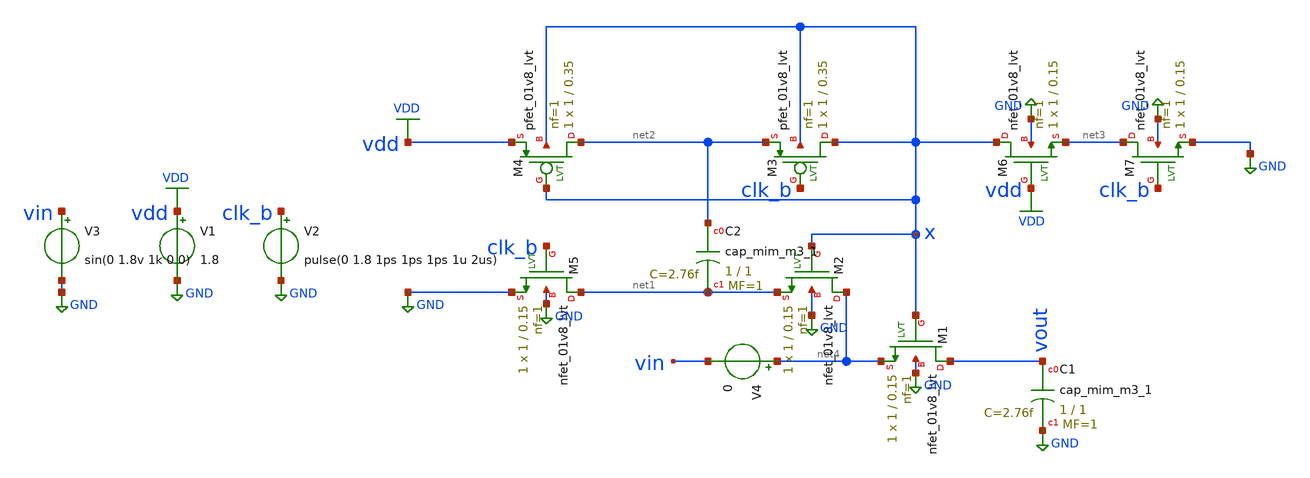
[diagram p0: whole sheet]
** sch_path: bootstrap.sch
**.subckt bootstrap
XM1 vout x net4 GND sky130_fd_pr__nfet_01v8_lvt L=0.15 W=1 nf=1 ad='int((nf+1)/2) * W/nf * 0.29' as='int((nf+2)/2) * W/nf * 0.29'
+ pd='2*int((nf+1)/2) * (W/nf + 0.29)' ps='2*int((nf+2)/2) * (W/nf + 0.29)' nrd='0.29 / W' nrs='0.29 / W'
+ sa=0 sb=0 sd=0 mult=1 m=1
XC1 vout GND sky130_fd_pr__cap_mim_m3_1 W=1 L=1 MF=1 m=1
XM2 net4 x net1 GND sky130_fd_pr__nfet_01v8_lvt L=0.15 W=1 nf=1 ad='int((nf+1)/2) * W/nf * 0.29' as='int((nf+2)/2) * W/nf * 0.29'
+ pd='2*int((nf+1)/2) * (W/nf + 0.29)' ps='2*int((nf+2)/2) * (W/nf + 0.29)' nrd='0.29 / W' nrs='0.29 / W'
+ sa=0 sb=0 sd=0 mult=1 m=1
XC2 net2 net1 sky130_fd_pr__cap_mim_m3_1 W=1 L=1 MF=1 m=1
XM3 x clk_b net2 x sky130_fd_pr__pfet_01v8_lvt L=0.35 W=1 nf=1 ad='int((nf+1)/2) * W/nf * 0.29' as='int((nf+2)/2) * W/nf * 0.29'
+ pd='2*int((nf+1)/2) * (W/nf + 0.29)' ps='2*int((nf+2)/2) * (W/nf + 0.29)' nrd='0.29 / W' nrs='0.29 / W'
+ sa=0 sb=0 sd=0 mult=1 m=1
XM4 net2 x VDD x sky130_fd_pr__pfet_01v8_lvt L=0.35 W=1 nf=1 ad='int((nf+1)/2) * W/nf * 0.29' as='int((nf+2)/2) * W/nf * 0.29'
+ pd='2*int((nf+1)/2) * (W/nf + 0.29)' ps='2*int((nf+2)/2) * (W/nf + 0.29)' nrd='0.29 / W' nrs='0.29 / W'
+ sa=0 sb=0 sd=0 mult=1 m=1
XM5 net1 clk_b GND GND sky130_fd_pr__nfet_01v8_lvt L=0.15 W=1 nf=1 ad='int((nf+1)/2) * W/nf * 0.29' as='int((nf+2)/2) * W/nf * 0.29'
+ pd='2*int((nf+1)/2) * (W/nf + 0.29)' ps='2*int((nf+2)/2) * (W/nf + 0.29)' nrd='0.29 / W' nrs='0.29 / W'
+ sa=0 sb=0 sd=0 mult=1 m=1
XM6 x VDD net3 GND sky130_fd_pr__nfet_01v8_lvt L=0.15 W=1 nf=1 ad='int((nf+1)/2) * W/nf * 0.29' as='int((nf+2)/2) * W/nf * 0.29'
+ pd='2*int((nf+1)/2) * (W/nf + 0.29)' ps='2*int((nf+2)/2) * (W/nf + 0.29)' nrd='0.29 / W' nrs='0.29 / W'
+ sa=0 sb=0 sd=0 mult=1 m=1
XM7 net3 clk_b GND GND sky130_fd_pr__nfet_01v8_lvt L=0.15 W=1 nf=1 ad='int((nf+1)/2) * W/nf * 0.29' as='int((nf+2)/2) * W/nf * 0.29'
+ pd='2*int((nf+1)/2) * (W/nf + 0.29)' ps='2*int((nf+2)/2) * (W/nf + 0.29)' nrd='0.29 / W' nrs='0.29 / W'
+ sa=0 sb=0 sd=0 mult=1 m=1
V1 VDD GND 1.8
V2 clk_b GND pulse(0 1.8 1ps 1ps 1ps 1u 2us)
V3 vin GND sin(0 1.8v 1k 0 0)
V4 net4 vin 0
**** begin user architecture code

.lib ~/open_pdks/sky130/sky130A/libs.tech/ngspice/sky130.lib.spice tt
*.param mc_mm_switch=0
*.param mc_pr_switch=0

*.include ~/open_pdks/sky130/sky130A/libs.tech/ngspice/corners/tt/nonfet.spice

*model
*.include ~/open_pdks/sky130/sky130A/libs.tech/ngspice/all.spice

*mosfet
*.include ~/open_pdks/sky130/sky130A/libs.ref/sky130_fd_pr/spice/sky130_fd_pr__pfet_01v8__tt.corner.spice
*.inclued ~/open_pdks/sky130/sky130A/libs.ref/sky130_fd_pr/spice/sky130_fd_pr__nfet_01v8__tt.corner.spice

*mismatch parameters
*.include ~/open_pdks/sky130/sky130A/libs.ref/sky130_fd_pr/spice/sky130_fd_pr__pfet_01v8__mismatch.corner.spice
*.include ~/open_pdks/sky130/sky130A/libs.ref/sky130_fd_pr/spice/sky130_fd_pr__nfet_01v8__mismatch.corner.spice

*mosfet
*.include ~/open_pdks/sky130/sky130A/libs.ref/sky130_fd_pr/spice/sky130_fd_pr__pfet_01v8_lvt__tt.corner.spice
*.inclued ~/open_pdks/sky130/sky130A/libs.ref/sky130_fd_pr/spice/sky130_fd_pr__nfet_01v8_lvt__tt.corner.spice

*mismatch parameters
*.include ~/open_pdks/sky130/sky130A/libs.ref/sky130_fd_pr/spice/sky130_fd_pr__pfet_01v8_lvt__mismatch.corner.spice
*.include ~/open_pdks/sky130/sky130A/libs.ref/sky130_fd_pr/spice/sky130_fd_pr__nfet_01v8_lvt__mismatch.corner.spice

.tran 0.1us 1ms
.save all


**** end user architecture code
**.ends
.GLOBAL GND
.GLOBAL VDD
.end
